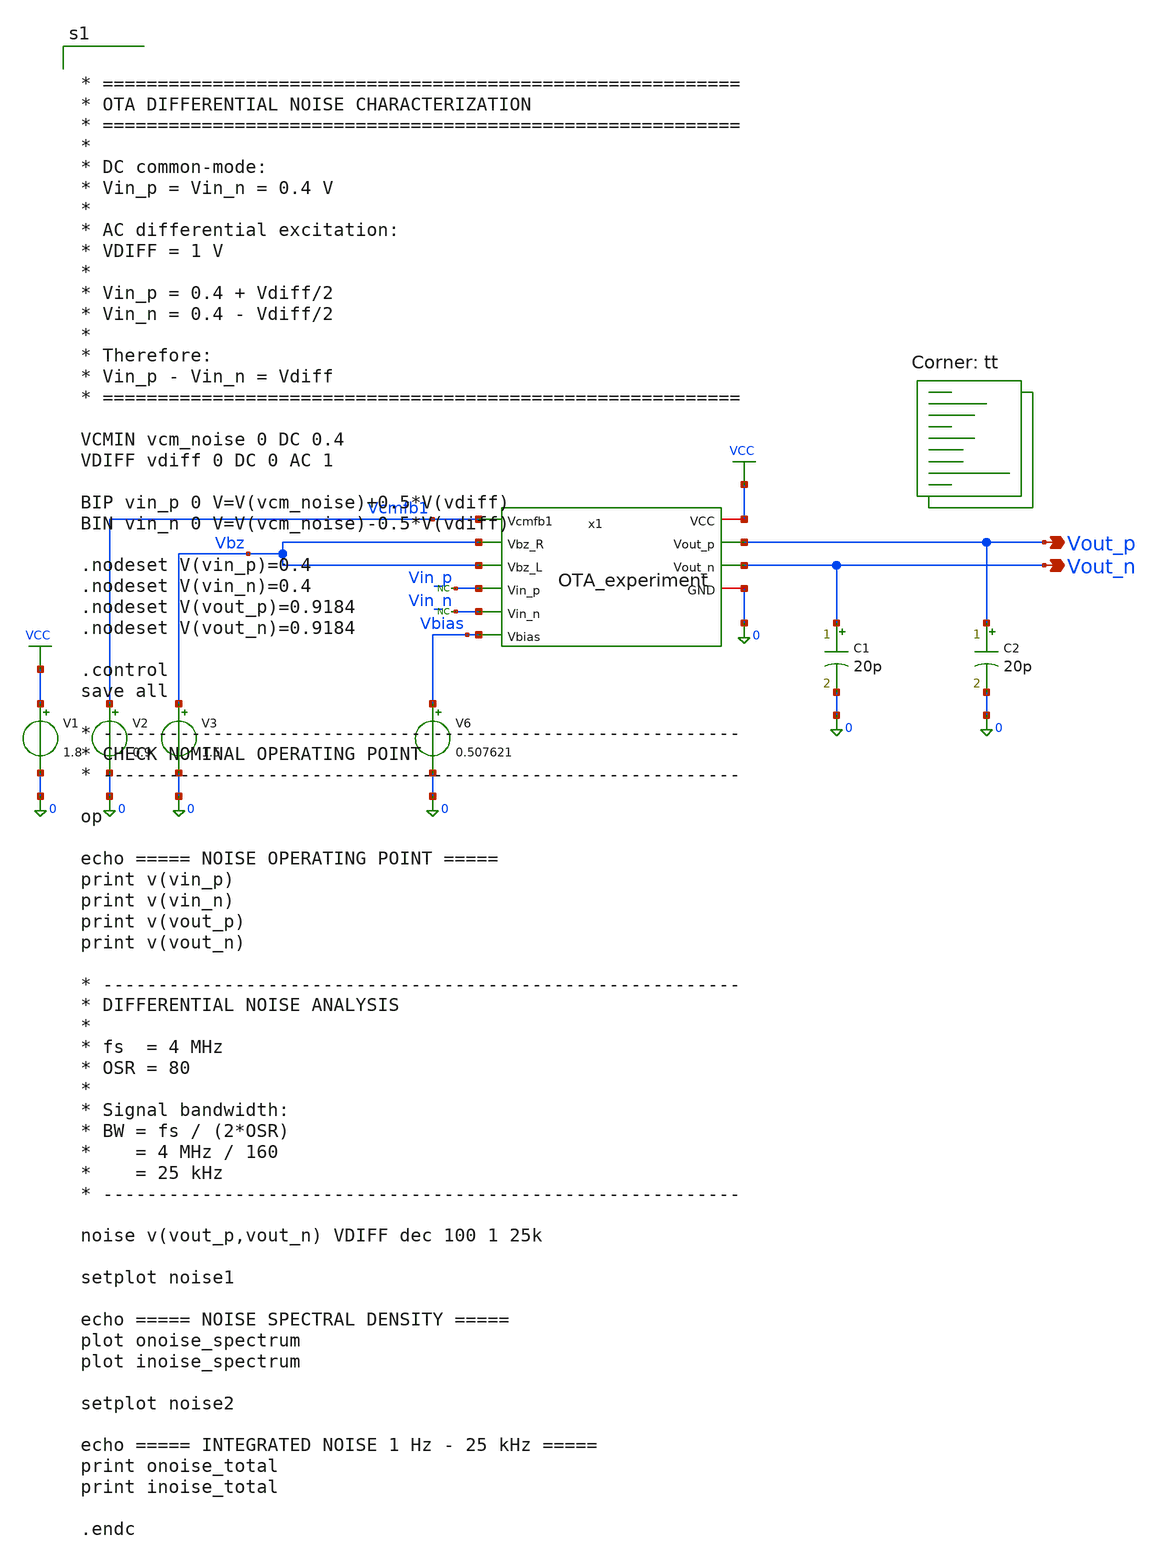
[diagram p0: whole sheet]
** sch_path: blocks/01_OTA/sim/tb_OTA_NOISE_experiment.sch
**.subckt tb_OTA_NOISE_experiment Vout_p Vout_n
*.opin Vout_p
*.opin Vout_n
V1 VCC 0 1.8
V2 Vcmfb1 0 0.9
V3 Vbz 0 1.5
V6 Vbias 0 0.507621
C1 Vout_n 0 20p m=1
C2 Vout_p 0 20p m=1
* noconn Vin_p
* noconn Vin_n
x1 VCC Vcmfb1 Vbz Vbz Vin_p Vin_n Vout_p Vout_n Vbias 0 OTA_experiment
**** begin user architecture code


* ==========================================================
* OTA DIFFERENTIAL NOISE CHARACTERIZATION
* ==========================================================
*
* DC common-mode:
* Vin_p = Vin_n = 0.4 V
*
* AC differential excitation:
* VDIFF = 1 V
*
* Vin_p = 0.4 + Vdiff/2
* Vin_n = 0.4 - Vdiff/2
*
* Therefore:
* Vin_p - Vin_n = Vdiff
* ==========================================================

VCMIN vcm_noise 0 DC 0.4
VDIFF vdiff 0 DC 0 AC 1

BIP vin_p 0 V=V(vcm_noise)+0.5*V(vdiff)
BIN vin_n 0 V=V(vcm_noise)-0.5*V(vdiff)

.nodeset V(vin_p)=0.4
.nodeset V(vin_n)=0.4
.nodeset V(vout_p)=0.9184
.nodeset V(vout_n)=0.9184

.control
save all

* ----------------------------------------------------------
* CHECK NOMINAL OPERATING POINT
* ----------------------------------------------------------

op

echo ===== NOISE OPERATING POINT =====
print v(vin_p)
print v(vin_n)
print v(vout_p)
print v(vout_n)

* ----------------------------------------------------------
* DIFFERENTIAL NOISE ANALYSIS
*
* fs  = 4 MHz
* OSR = 80
*
* Signal bandwidth:
* BW = fs / (2*OSR)
*    = 4 MHz / 160
*    = 25 kHz
* ----------------------------------------------------------

noise v(vout_p,vout_n) VDIFF dec 100 1 25k

setplot noise1

echo ===== NOISE SPECTRAL DENSITY =====
plot onoise_spectrum
plot inoise_spectrum

setplot noise2

echo ===== INTEGRATED NOISE 1 Hz - 25 kHz =====
print onoise_total
print inoise_total

.endc


.lib $::SKYWATER_MODELS/sky130.lib.spice tt
**** end user architecture code
**.ends

* expanding   symbol:  blocks/01_OTA/xschem/OTA_experiment.sym # of pins=10
** sym_path: blocks/01_OTA/xschem/OTA_experiment.sym
** sch_path: blocks/01_OTA/xschem/OTA_experiment.sch
.subckt OTA_experiment VCC Vcmfb1 Vbz_R Vbz_L Vin_p Vin_n Vout_p Vout_n Vbias GND
*.ipin Vin_p
*.ipin Vin_n
*.ipin Vbias
*.ipin Vbz_R
*.ipin Vbz_L
*.ipin Vcmfb1
*.opin Vout_p
*.opin Vout_n
*.iopin VCC
*.iopin GND
XM1 net5 Vin_p net3 net5 sky130_fd_pr__pfet_01v8 L=1.2 W=120 nf=1 ad='int((1 + 1)/2) * 120 / 1 * 0.29'
+ as='int((1 + 2)/2) * 120 / 1 * 0.29' pd='2*int((1 + 1)/2) * (120 / 1 + 0.29)' ps='2*int((1 + 2)/2) * (120 / 1 + 0.29)'
+ nrd='0.29 / 120 ' nrs='0.29 / 120 ' sa=0 sb=0 sd=0 mult=1 m=1
XM2 net5 Vin_n net4 net5 sky130_fd_pr__pfet_01v8 L=1.2 W=120 nf=1 ad='int((1 + 1)/2) * 120 / 1 * 0.29'
+ as='int((1 + 2)/2) * 120 / 1 * 0.29' pd='2*int((1 + 1)/2) * (120 / 1 + 0.29)' ps='2*int((1 + 2)/2) * (120 / 1 + 0.29)'
+ nrd='0.29 / 120 ' nrs='0.29 / 120 ' sa=0 sb=0 sd=0 mult=1 m=1
XM3 net3 Vbias GND GND sky130_fd_pr__nfet_01v8 L=2 W=8 nf=1 ad='int((1 + 1)/2) * 8 / 1 * 0.29' as='int((1 + 2)/2) * 8 / 1 * 0.29'
+ pd='2*int((1 + 1)/2) * (8 / 1 + 0.29)' ps='2*int((1 + 2)/2) * (8 / 1 + 0.29)' nrd='0.29 / 8 ' nrs='0.29 / 8 '
+ sa=0 sb=0 sd=0 mult=1 m=1
XM4 net4 Vbias GND GND sky130_fd_pr__nfet_01v8 L=2 W=8 nf=1 ad='int((1 + 1)/2) * 8 / 1 * 0.29' as='int((1 + 2)/2) * 8 / 1 * 0.29'
+ pd='2*int((1 + 1)/2) * (8 / 1 + 0.29)' ps='2*int((1 + 2)/2) * (8 / 1 + 0.29)' nrd='0.29 / 8 ' nrs='0.29 / 8 '
+ sa=0 sb=0 sd=0 mult=1 m=1
XM5 net1 net4 GND GND sky130_fd_pr__nfet_01v8 L=2 W=20 nf=1 ad='int((1 + 1)/2) * 20 / 1 * 0.29' as='int((1 + 2)/2) * 20 / 1 * 0.29'
+ pd='2*int((1 + 1)/2) * (20 / 1 + 0.29)' ps='2*int((1 + 2)/2) * (20 / 1 + 0.29)' nrd='0.29 / 20 ' nrs='0.29 / 20 '
+ sa=0 sb=0 sd=0 mult=1 m=1
XM6 net2 net3 GND GND sky130_fd_pr__nfet_01v8 L=2 W=20 nf=1 ad='int((1 + 1)/2) * 20 / 1 * 0.29' as='int((1 + 2)/2) * 20 / 1 * 0.29'
+ pd='2*int((1 + 1)/2) * (20 / 1 + 0.29)' ps='2*int((1 + 2)/2) * (20 / 1 + 0.29)' nrd='0.29 / 20 ' nrs='0.29 / 20 '
+ sa=0 sb=0 sd=0 mult=1 m=1
XM7 VCC net1 net1 VCC sky130_fd_pr__pfet_01v8 L=2 W=30 nf=1 ad='int((1 + 1)/2) * 30 / 1 * 0.29' as='int((1 + 2)/2) * 30 / 1 * 0.29'
+ pd='2*int((1 + 1)/2) * (30 / 1 + 0.29)' ps='2*int((1 + 2)/2) * (30 / 1 + 0.29)' nrd='0.29 / 30 ' nrs='0.29 / 30 '
+ sa=0 sb=0 sd=0 mult=1 m=1
XM8 VCC net2 net2 VCC sky130_fd_pr__pfet_01v8 L=2 W=30 nf=1 ad='int((1 + 1)/2) * 30 / 1 * 0.29' as='int((1 + 2)/2) * 30 / 1 * 0.29'
+ pd='2*int((1 + 1)/2) * (30 / 1 + 0.29)' ps='2*int((1 + 2)/2) * (30 / 1 + 0.29)' nrd='0.29 / 30 ' nrs='0.29 / 30 '
+ sa=0 sb=0 sd=0 mult=1 m=1
XM9 VCC net1 Vout_p VCC sky130_fd_pr__pfet_01v8 L=1 W=300 nf=1 ad='int((1 + 1)/2) * 300 / 1 * 0.29' as='int((1 + 2)/2) * 300 / 1 * 0.29'
+ pd='2*int((1 + 1)/2) * (300 / 1 + 0.29)' ps='2*int((1 + 2)/2) * (300 / 1 + 0.29)' nrd='0.29 / 300 ' nrs='0.29 / 300 '
+ sa=0 sb=0 sd=0 mult=1 m=1
XM10 VCC net2 Vout_n VCC sky130_fd_pr__pfet_01v8 L=1 W=300 nf=1 ad='int((1 + 1)/2) * 300 / 1 * 0.29'
+ as='int((1 + 2)/2) * 300 / 1 * 0.29' pd='2*int((1 + 1)/2) * (300 / 1 + 0.29)' ps='2*int((1 + 2)/2) * (300 / 1 + 0.29)'
+ nrd='0.29 / 300 ' nrs='0.29 / 300 ' sa=0 sb=0 sd=0 mult=1 m=1
XM11 Vout_p net4 GND GND sky130_fd_pr__nfet_01v8 L=1 W=200 nf=1 ad='int((1 + 1)/2) * 200 / 1 * 0.29'
+ as='int((1 + 2)/2) * 200 / 1 * 0.29' pd='2*int((1 + 1)/2) * (200 / 1 + 0.29)' ps='2*int((1 + 2)/2) * (200 / 1 + 0.29)'
+ nrd='0.29 / 200 ' nrs='0.29 / 200 ' sa=0 sb=0 sd=0 mult=1 m=1
XM12 Vout_n net3 GND GND sky130_fd_pr__nfet_01v8 L=1 W=200 nf=1 ad='int((1 + 1)/2) * 200 / 1 * 0.29'
+ as='int((1 + 2)/2) * 200 / 1 * 0.29' pd='2*int((1 + 1)/2) * (200 / 1 + 0.29)' ps='2*int((1 + 2)/2) * (200 / 1 + 0.29)'
+ nrd='0.29 / 200 ' nrs='0.29 / 200 ' sa=0 sb=0 sd=0 mult=1 m=1
XM13 VCC Vcmfb1 net5 VCC sky130_fd_pr__pfet_01v8 L=1.2 W=60 nf=1 ad='int((1 + 1)/2) * 60 / 1 * 0.29'
+ as='int((1 + 2)/2) * 60 / 1 * 0.29' pd='2*int((1 + 1)/2) * (60 / 1 + 0.29)' ps='2*int((1 + 2)/2) * (60 / 1 + 0.29)'
+ nrd='0.29 / 60 ' nrs='0.29 / 60 ' sa=0 sb=0 sd=0 mult=1 m=1
XC1 Vout_p net4 sky130_fd_pr__cap_mim_m3_1 W=1 L=1 MF=80 m=80
XC2 net3 Vout_n sky130_fd_pr__cap_mim_m3_1 W=1 L=1 MF=80 m=80
.ends

.GLOBAL VCC
.end
